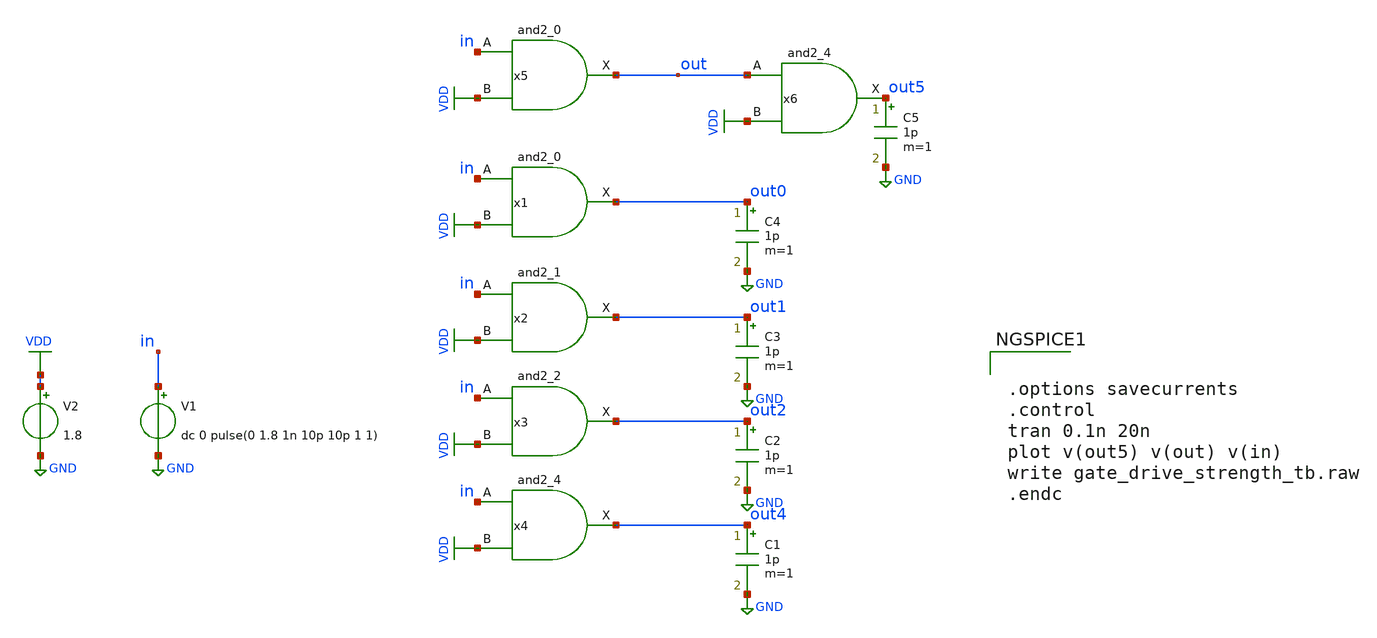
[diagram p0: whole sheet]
** sch_path: verification/analog_modulator/gate_drive_strength_tb.sch
**.subckt gate_drive_strength_tb
V2 VDD GND 1.8
V1 in GND dc 0 pulse(0 1.8 1n 10p 10p 1 1)
C1 out4 GND 1p m=1
x1 in VDD GND GND VDD VDD out0 sky130_fd_sc_hd__and2_0
x2 in VDD GND GND VDD VDD out1 sky130_fd_sc_hd__and2_1
x3 in VDD GND GND VDD VDD out2 sky130_fd_sc_hd__and2_2
x4 in VDD GND GND VDD VDD out4 sky130_fd_sc_hd__and2_4
C2 out2 GND 1p m=1
C3 out1 GND 1p m=1
C4 out0 GND 1p m=1
x5 in VDD GND GND VDD VDD out sky130_fd_sc_hd__and2_0
x6 out VDD GND GND VDD VDD out5 sky130_fd_sc_hd__and2_4
C5 out5 GND 1p m=1
**** begin user architecture code


.options savecurrents
.control
tran 0.1n 20n
plot v(out5) v(out) v(in)
write gate_drive_strength_tb.raw
.endc



** opencircuitdesign pdks install
.lib /farmshare/home/classes/ee/372/PDKs/open_pdks_1.0.310/sky130/sky130A/libs.tech/ngspice/sky130.lib.spice tt
.inc /farmshare/home/classes/ee/372/PDKs/open_pdks_1.0.310/sky130/sky130A/libs.ref/sky130_fd_sc_hd/spice/sky130_fd_sc_hd.spice

**** end user architecture code
**.ends
.GLOBAL GND
.GLOBAL VDD
.end
